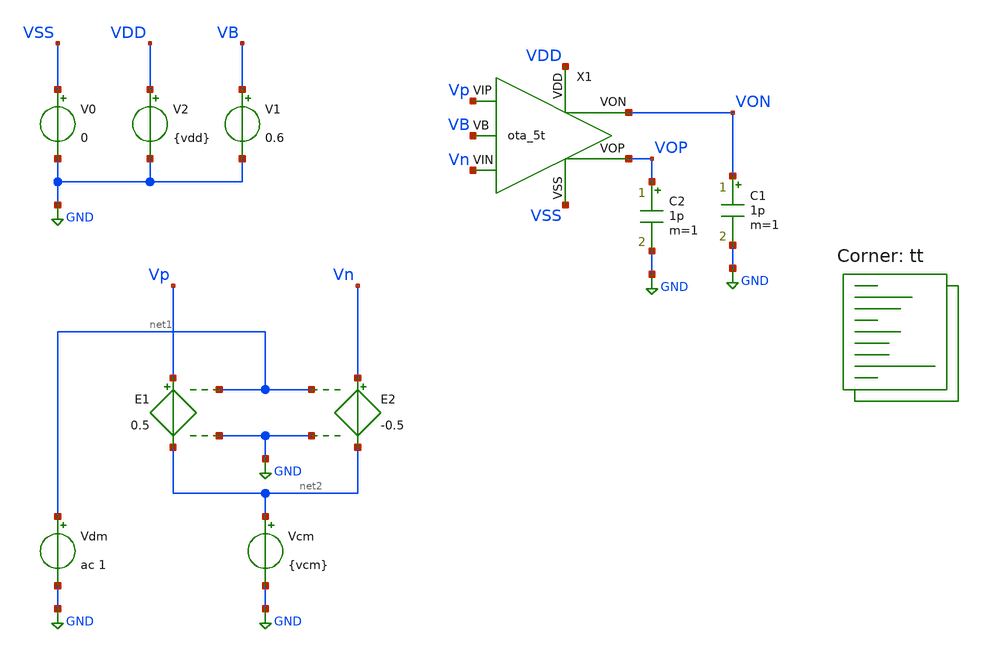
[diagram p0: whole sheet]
** sch_path: xschem/preamp/ota_5t_tb.sch
**.subckt ota_5t_tb
C1 VON GND 1p m=1
V0 VSS GND 0
V2 VDD GND {vdd}
E1 Vp net2 net1 GND 0.5
E2 Vn net2 net1 GND -0.5
Vdm net1 GND ac 1
Vcm net2 GND {vcm}
X1 VB Vn Vp VOP VDD VSS VON ota_5t
C2 VOP GND 1p m=1
V1 VB GND 0.6
**** begin user architecture code


.param vdd=1.8
.param vcm=0.9

.control

    save all

    * operating point
    op

    write ota_5t_tb.raw
    set appendwrite

    * run ac simulation
    ac dec 20 1k 100e6

    * measure parameters
    let vout_mag = abs(v(VOP)-v(VON))
    let vout_phase_margin = phase(v(VOP)-v(VON)) * 180/pi + 180
    meas ac A0 find vout_mag at=1k
    meas ac UGF when vout_mag=1 fall=1
    meas ac PM find vout_phase_margin when vout_mag=1

    write ota_5t_tb.raw
    quit 0
.endc


.lib $::SKYWATER_MODELS/sky130.lib.spice tt
**** end user architecture code
**.ends

* expanding   symbol:  xschem/preamp/ota_5t.sym # of pins=7
** sym_path: xschem/preamp/ota_5t.sym
** sch_path: xschem/preamp/ota_5t.sch
.subckt ota_5t VB VIN VIP VOP VDD VSS VON
*.iopin VDD
*.iopin VSS
*.opin VOP
*.ipin VIP
*.ipin VIN
*.ipin VB
*.opin VON
XM3 VON VIP net1 VSS sky130_fd_pr__nfet_01v8 L=1 W=5 nf=2 ad='int((2 + 1)/2) * 5 / 2 * 0.29' as='int((2 + 2)/2) * 5 / 2 * 0.29'
+ pd='2*int((2 + 1)/2) * (5 / 2 + 0.29)' ps='2*int((2 + 2)/2) * (5 / 2 + 0.29)' nrd='0.29 / 5 ' nrs='0.29 / 5 '
+ sa=0 sb=0 sd=0 mult=1 m=1
XM1 VOP VOP VDD VDD sky130_fd_pr__pfet_01v8 L=2.5 W=1.5 nf=2 ad='int((nf+1)/2) * W/nf * 0.29' as='int((nf+2)/2) * W/nf * 0.29'
+ pd='2*int((nf+1)/2) * (W/nf + 0.29)' ps='2*int((nf+2)/2) * (W/nf + 0.29)' nrd='0.29 / W' nrs='0.29 / W'
+ sa=0 sb=0 sd=0 mult=1 m=1
XM4 VOP VIN net1 VSS sky130_fd_pr__nfet_01v8 L=1 W=5 nf=2 ad='int((2 + 1)/2) * 5 / 2 * 0.29' as='int((2 + 2)/2) * 5 / 2 * 0.29'
+ pd='2*int((2 + 1)/2) * (5 / 2 + 0.29)' ps='2*int((2 + 2)/2) * (5 / 2 + 0.29)' nrd='0.29 / 5 ' nrs='0.29 / 5 '
+ sa=0 sb=0 sd=0 mult=1 m=1
XM5 net1 VB VSS VSS sky130_fd_pr__nfet_01v8 L=0.15 W=2 nf=1 ad='int((1 + 1)/2) * 2 / 1 * 0.29' as='int((1 + 2)/2) * 2 / 1 * 0.29'
+ pd='2*int((1 + 1)/2) * (2 / 1 + 0.29)' ps='2*int((1 + 2)/2) * (2 / 1 + 0.29)' nrd='0.29 / 2 ' nrs='0.29 / 2 '
+ sa=0 sb=0 sd=0 mult=1 m=1
XM8 VON VON VDD VDD sky130_fd_pr__pfet_01v8 L=2.5 W=1.5 nf=2 ad='int((nf+1)/2) * W/nf * 0.29' as='int((nf+2)/2) * W/nf * 0.29'
+ pd='2*int((nf+1)/2) * (W/nf + 0.29)' ps='2*int((nf+2)/2) * (W/nf + 0.29)' nrd='0.29 / W' nrs='0.29 / W'
+ sa=0 sb=0 sd=0 mult=1 m=1
.ends

.GLOBAL GND
.end
